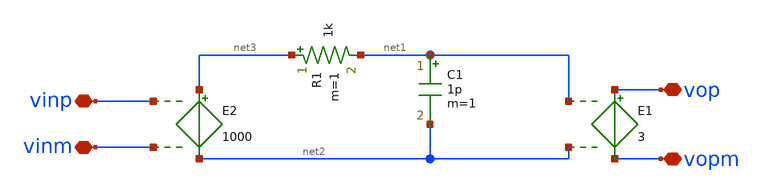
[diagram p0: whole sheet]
** sch_path: work/xschem/untitled-1.sch
**.subckt untitled-1 vinp vinm vop vopm
*.iopin vinp
*.iopin vinm
*.iopin vop
*.iopin vopm
E1 vop vopm net1 net2 3
E2 net3 net2 vinp vinm 1000
R1 net3 net1 1k m=1
C1 net1 net2 1p m=1
**.ends
.end
